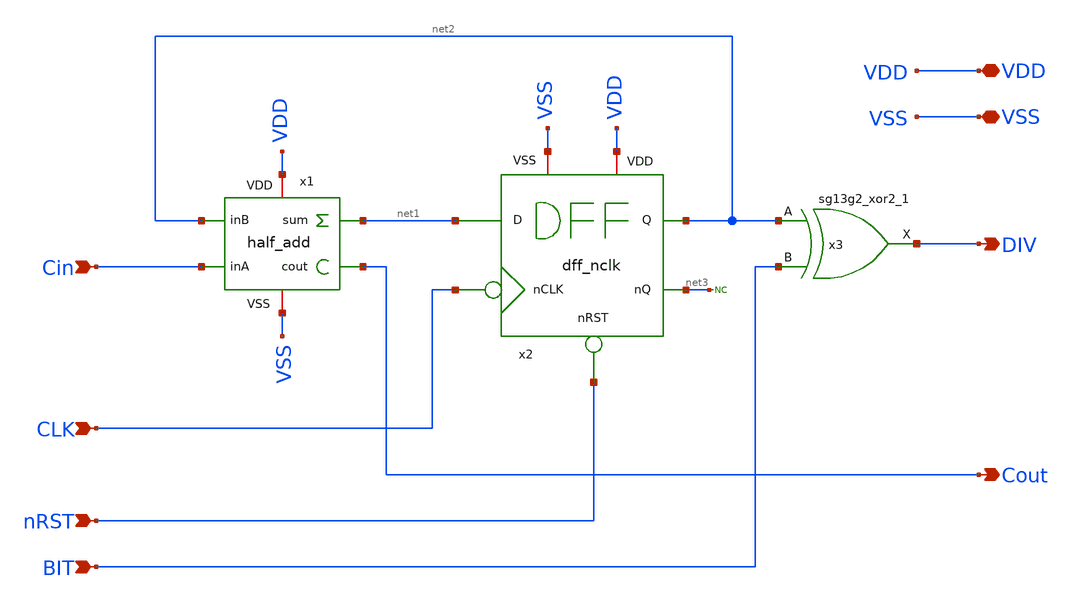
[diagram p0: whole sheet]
** sch_path: Combined_Design/design_data/xschem/freq_div_cell.sch
**.subckt freq_div_cell Cin CLK nRST BIT DIV Cout VSS VDD
*.ipin Cin
*.ipin CLK
*.ipin nRST
*.ipin BIT
*.opin DIV
*.opin Cout
*.iopin VSS
*.iopin VDD
x2 CLK net2 net1 net3 nRST VDD VSS dff_nclk
x3 DIV net2 BIT VDD VSS sg13g2_xor2_1
* noconn #net3
x1 net2 net1 Cin VDD VSS Cout half_add
**.ends

* expanding   symbol:  sg13g2_stdcells/sg13g2_xor2_1.sym # of pins=3
** sym_path: sg13g2_stdcells/sg13g2_xor2_1.sym
** sch_path: sg13g2_stdcells/sg13g2_xor2_1.sch
.subckt sg13g2_xor2_1 X A B VDD VSS
*.opin X
*.ipin B
*.ipin A
*.iopin VDD
*.iopin VSS
XM1 net1 A VSS VSS sg13_lv_nmos w=550.00n l=130.00n ng=1 m=1 mm_ok=1
XM2 net1 B VSS VSS sg13_lv_nmos w=550.00n l=130.00n ng=1 m=1 mm_ok=1
XM3 X net1 VSS VSS sg13_lv_nmos w=740.00n l=130.00n ng=1 m=1 mm_ok=1
XM4 X B net3 VSS sg13_lv_nmos w=740.00n l=130.00n ng=1 m=1 mm_ok=1
XM5 net3 A VSS VSS sg13_lv_nmos w=740.00n l=130.00n ng=1 m=1 mm_ok=1
XM6 net4 A VDD VDD sg13_lv_pmos w=1.000u l=130.00n ng=1 m=1 mm_ok=1
XM7 net1 B net4 VDD sg13_lv_pmos w=1.000u l=130.00n ng=1 m=1 mm_ok=1
XM8 net2 A VDD VDD sg13_lv_pmos w=1.12u l=130.00n ng=1 m=1 mm_ok=1
XM9 X net1 net2 VDD sg13_lv_pmos w=1.12u l=130.00n ng=1 m=1 mm_ok=1
XM10 net2 B VDD VDD sg13_lv_pmos w=1.12u l=130.00n ng=1 m=1 mm_ok=1
.ends

.end
